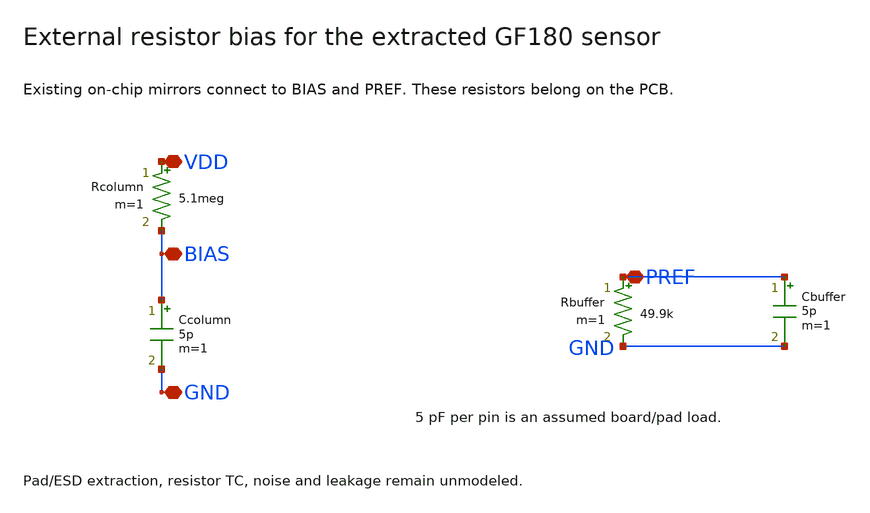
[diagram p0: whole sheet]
** sch_path: xschem/board_bias.sch
**.subckt board_bias VDD GND BIAS PREF
*.iopin VDD
*.iopin GND
*.iopin BIAS
*.iopin PREF
Rcolumn VDD BIAS 5.1meg m=1
Ccolumn BIAS GND 5p m=1
Rbuffer PREF GND 49.9k m=1
Cbuffer PREF GND 5p m=1
**.ends
.end
